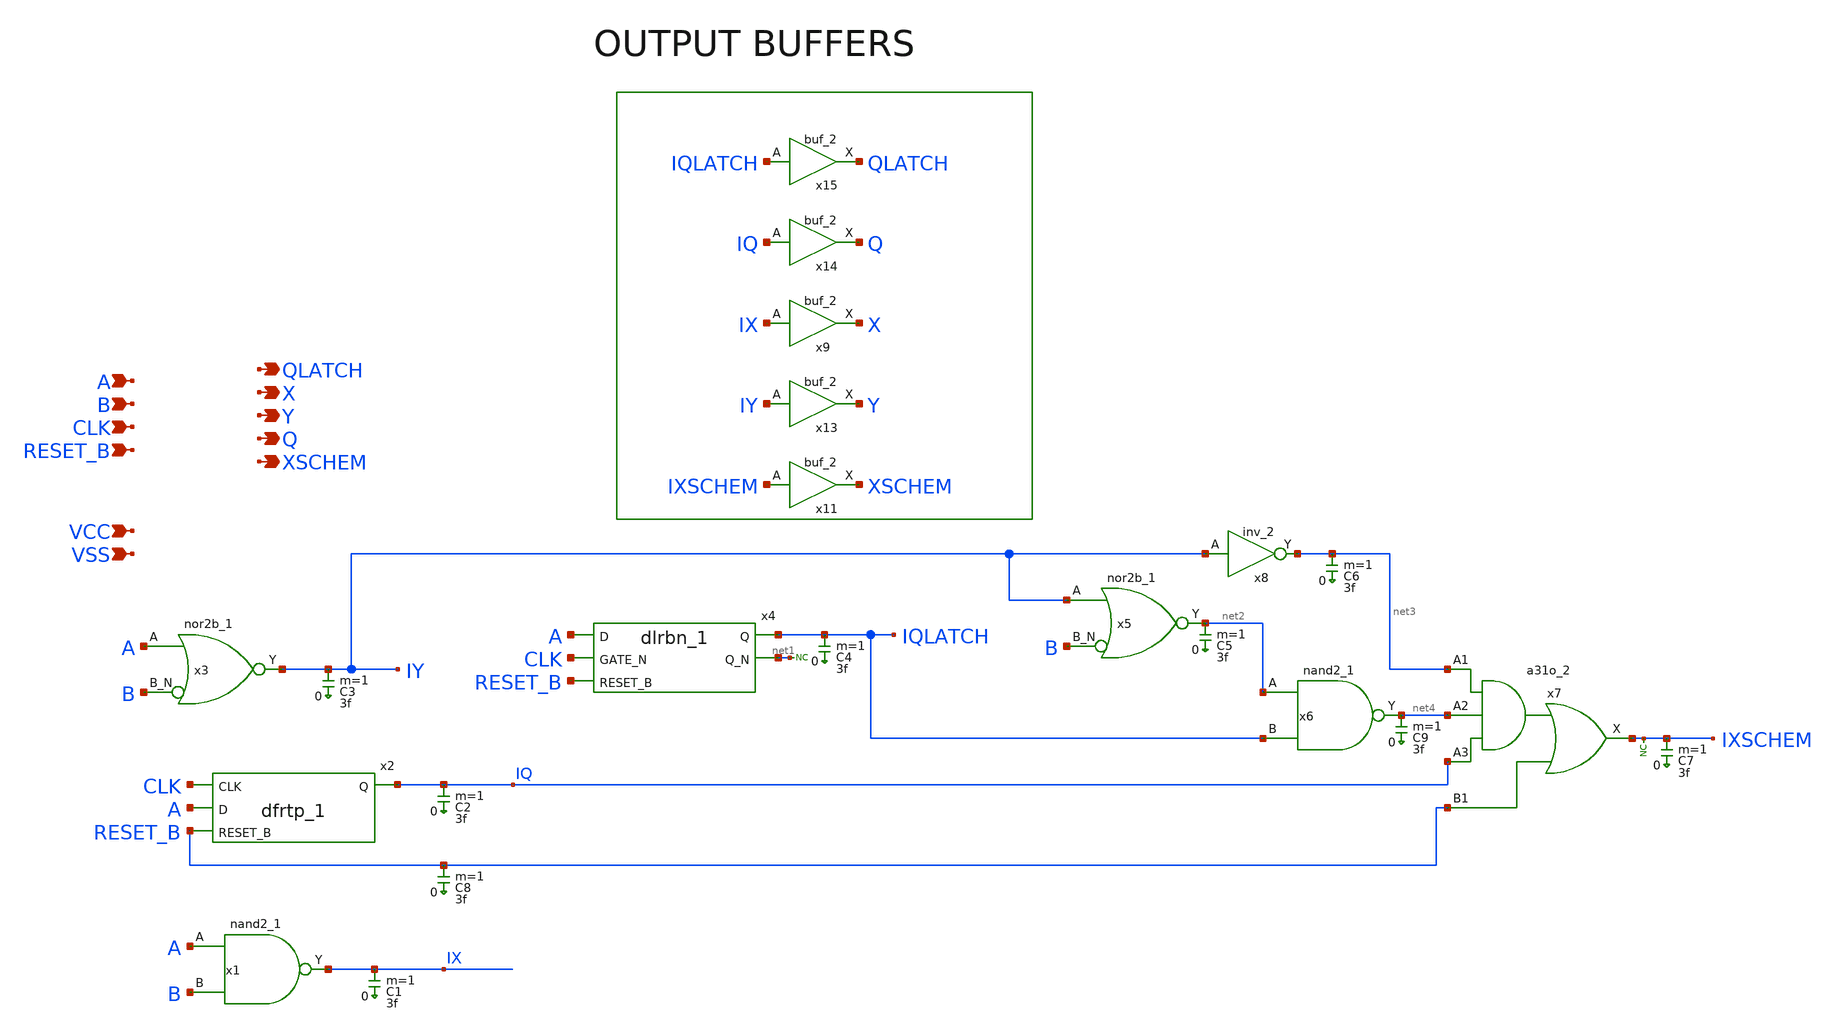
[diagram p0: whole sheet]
** sch_path: sky130A/xschem_libs/sky130_tests/stdcells/schematic/stdcells.sch
* Copyright 2021 Stefan Frederik Schippers
* Licensed under the Apache License, Version 2.0 (the "License");
* you may not use this file except in compliance with the License.
* You may obtain a copy of the License at
* https://www.apache.org/licenses/LICENSE-2.0
* Unless required by applicable law or agreed to in writing, software
* distributed under the License is distributed on an "AS IS" BASIS,
* WITHOUT WARRANTIES OR CONDITIONS OF ANY KIND, either express or implied.
* See the License for the specific language governing permissions and
* limitations under the License.
**.subckt stdcells RESET_B CLK B A Y X QLATCH Q XSCHEM VCC VSS
*.ipin RESET_B
*.ipin CLK
*.ipin B
*.ipin A
*.opin Y
*.opin X
*.opin QLATCH
*.opin Q
*.opin XSCHEM
*.ipin VCC
*.ipin VSS
x1 A B VSS VSS VCC VCC IX sky130_fd_sc_hd__nand2_1
C1 IX 0 3f m=1
x2 CLK A RESET_B VSS VSS VCC VCC IQ sky130_fd_sc_hd__dfrtp_1
C2 IQ 0 3f m=1
C3 IY 0 3f m=1
x3 A B VSS VSS VCC VCC IY sky130_fd_sc_hd__nor2b_1
x4 A CLK RESET_B VSS VSS VCC VCC IQLATCH net1 sky130_fd_sc_hd__dlrbn_1
C4 IQLATCH 0 3f m=1
x5 IY B VSS VSS VCC VCC net2 sky130_fd_sc_hd__nor2b_1
x6 net2 IQLATCH VSS VSS VCC VCC net4 sky130_fd_sc_hd__nand2_1
x7 net3 net4 IQ RESET_B VSS VSS VCC VCC IXSCHEM sky130_fd_sc_hd__a31o_2
* noconn #net1
* noconn IXSCHEM
x8 IY VSS VSS VCC VCC net3 sky130_fd_sc_hd__inv_2
x13 IY VSS VSS VCC VCC Y sky130_fd_sc_hd__buf_2
x9 IX VSS VSS VCC VCC X sky130_fd_sc_hd__buf_2
x14 IQ VSS VSS VCC VCC Q sky130_fd_sc_hd__buf_2
x15 IQLATCH VSS VSS VCC VCC QLATCH sky130_fd_sc_hd__buf_2
x11 IXSCHEM VSS VSS VCC VCC XSCHEM sky130_fd_sc_hd__buf_2
C5 net2 0 3f m=1
C6 net3 0 3f m=1
C7 IXSCHEM 0 3f m=1
C8 RESET_B 0 3f m=1
C9 net4 0 3f m=1
**.ends
.end
